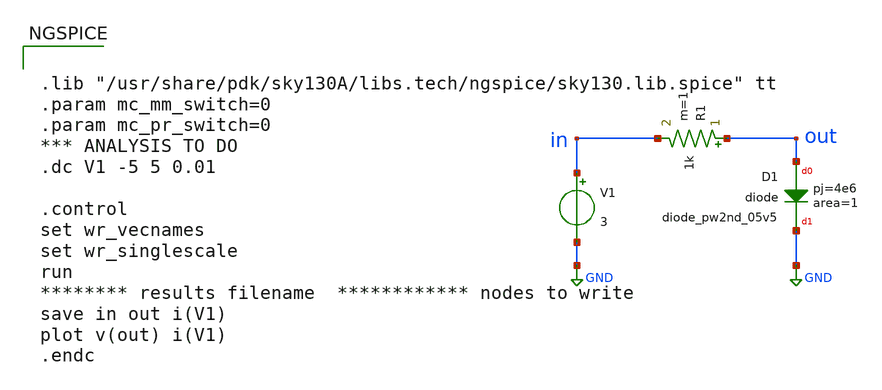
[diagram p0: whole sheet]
** sch_path: dev/esd_cell/tb/dIV05/dIV05.sch
**.subckt dIV05
XD1 out GND sky130_fd_pr__diode_pw2nd_05v5 area=1 pj=4e6
V1 in GND 3
R1 out in 1k m=1
**** begin user architecture code


.lib "/usr/share/pdk/sky130A/libs.tech/ngspice/sky130.lib.spice" tt
.param mc_mm_switch=0
.param mc_pr_switch=0
*** ANALYSIS TO DO
.dc V1 -5 5 0.01

.control
set wr_vecnames
set wr_singlescale
run
******** results filename  ************ nodes to write
save in out i(V1)
plot v(out) i(V1)
.endc


**** end user architecture code
**.ends
.GLOBAL GND
.end
